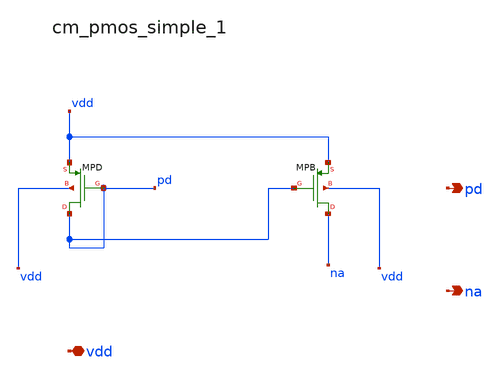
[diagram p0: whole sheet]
** sch_path: analog-db/raw/buf_001_super_follower/hier/blocks/cm_pmos_simple_1.sch
**.subckt cm_pmos_simple_1 vdd pd na
*.iopin vdd
*.opin pd
*.opin na
XMPB na pd vdd vdd sg13_lv_pmos w=x_dut_xmpb_w l=x_dut_xmpb_l ng=1 m=x_dut_xmpb_m
XMPD pd pd vdd vdd sg13_lv_pmos w=x_dut_xmpd_w l=x_dut_xmpd_l ng=1 m=x_dut_xmpd_m
**.ends
.end
